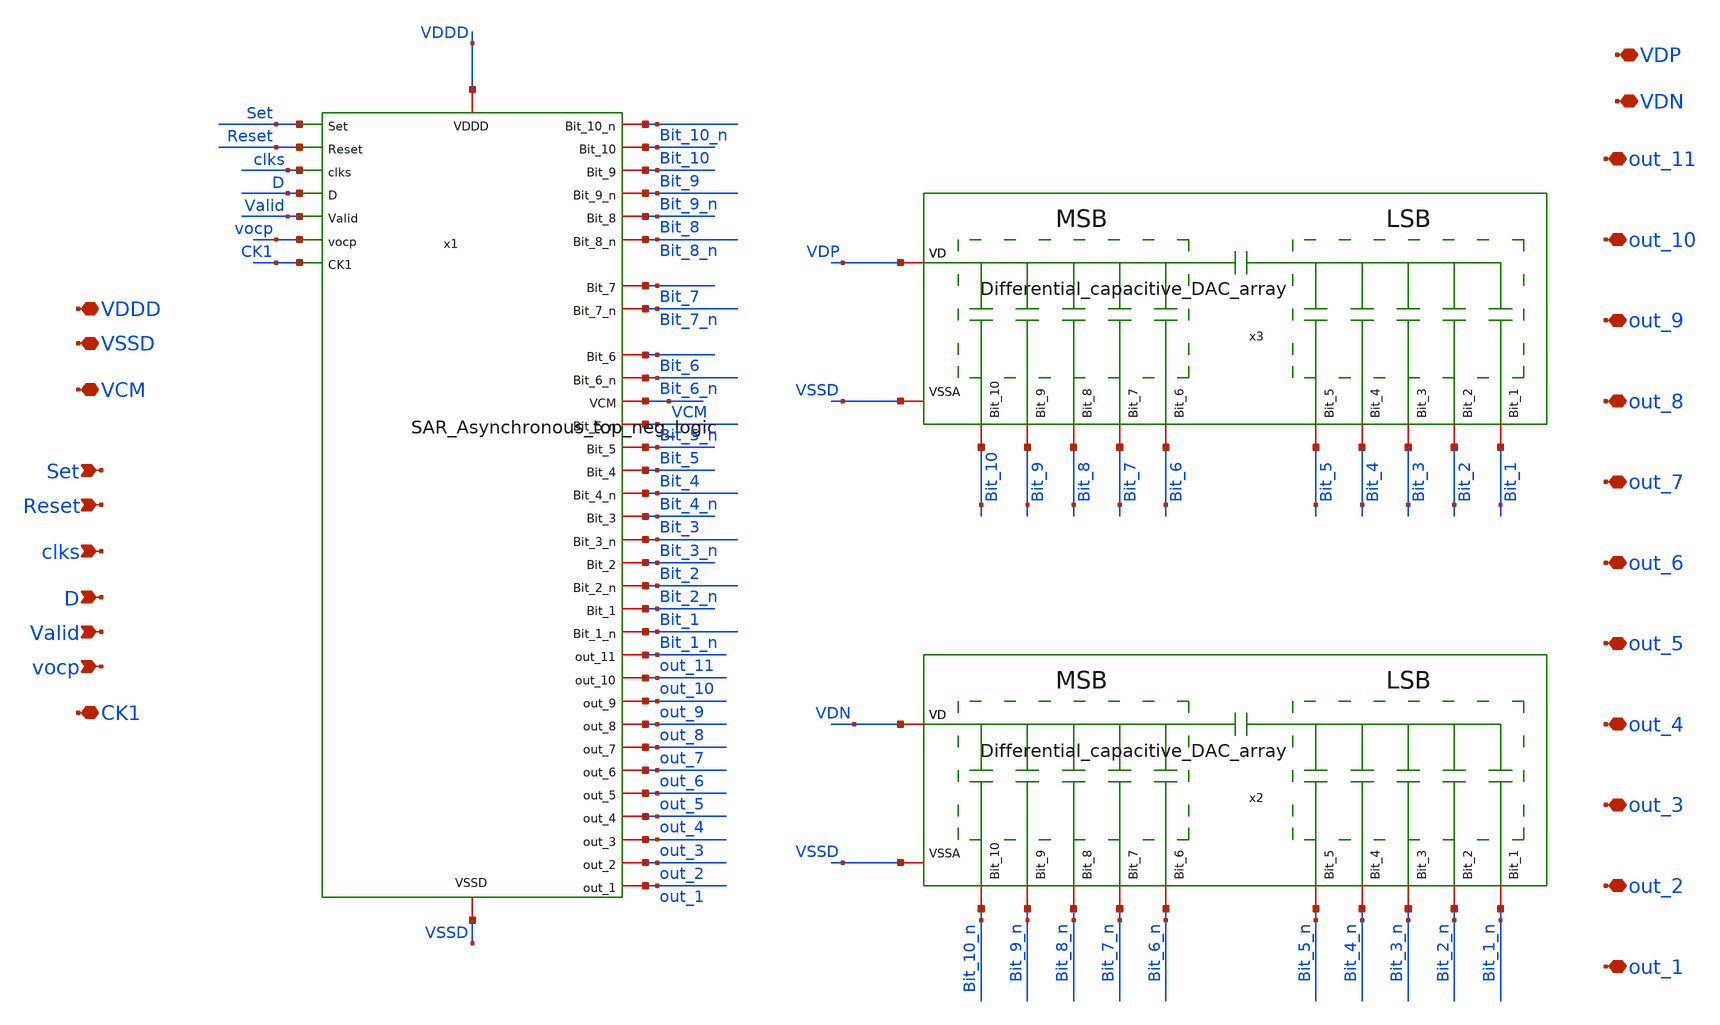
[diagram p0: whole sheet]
** sch_path: SAR_ADC/SAR_logic_dac/SAR_logic_dac.sch
**.subckt SAR_logic_dac VDDD VSSD Set Reset VCM clks D Valid vocp out_11 out_10 out_9 out_8 out_7
*+ out_6 out_5 out_4 out_3 out_2 out_1 VDN VDP CK1
*.iopin VDDD
*.iopin VSSD
*.ipin Set
*.ipin Reset
*.iopin VCM
*.ipin clks
*.ipin D
*.ipin Valid
*.ipin vocp
*.iopin out_11
*.iopin out_10
*.iopin out_9
*.iopin out_8
*.iopin out_7
*.iopin out_6
*.iopin out_5
*.iopin out_4
*.iopin out_3
*.iopin out_2
*.iopin out_1
*.iopin VDN
*.iopin VDP
*.iopin CK1
x1 Bit_10_n Bit_10 Bit_9 Bit_9_n Bit_8 Bit_8_n VDDD Bit_7 Bit_7_n VSSD Bit_6 Bit_6_n VCM Bit_5_n
+ Bit_5 Bit_4 Bit_4_n Set Bit_3 Bit_3_n Reset Bit_2 Bit_2_n clks Bit_1 Bit_1_n D Valid out_11 vocp out_10
+ out_9 out_8 out_7 out_6 out_5 out_4 out_3 out_2 out_1 CK1 SAR_Asynchronous_top_neg_logic
x2 VDN Bit_3_n Bit_8_n Bit_5_n Bit_6_n Bit_7_n Bit_4_n Bit_9_n Bit_10_n Bit_2_n Bit_1_n VSSD
+ Differential_capacitive_DAC_array
x3 VDP Bit_3 Bit_8 Bit_5 Bit_6 Bit_7 Bit_4 Bit_9 Bit_10 Bit_2 Bit_1 VSSD
+ Differential_capacitive_DAC_array
**.ends
.end
